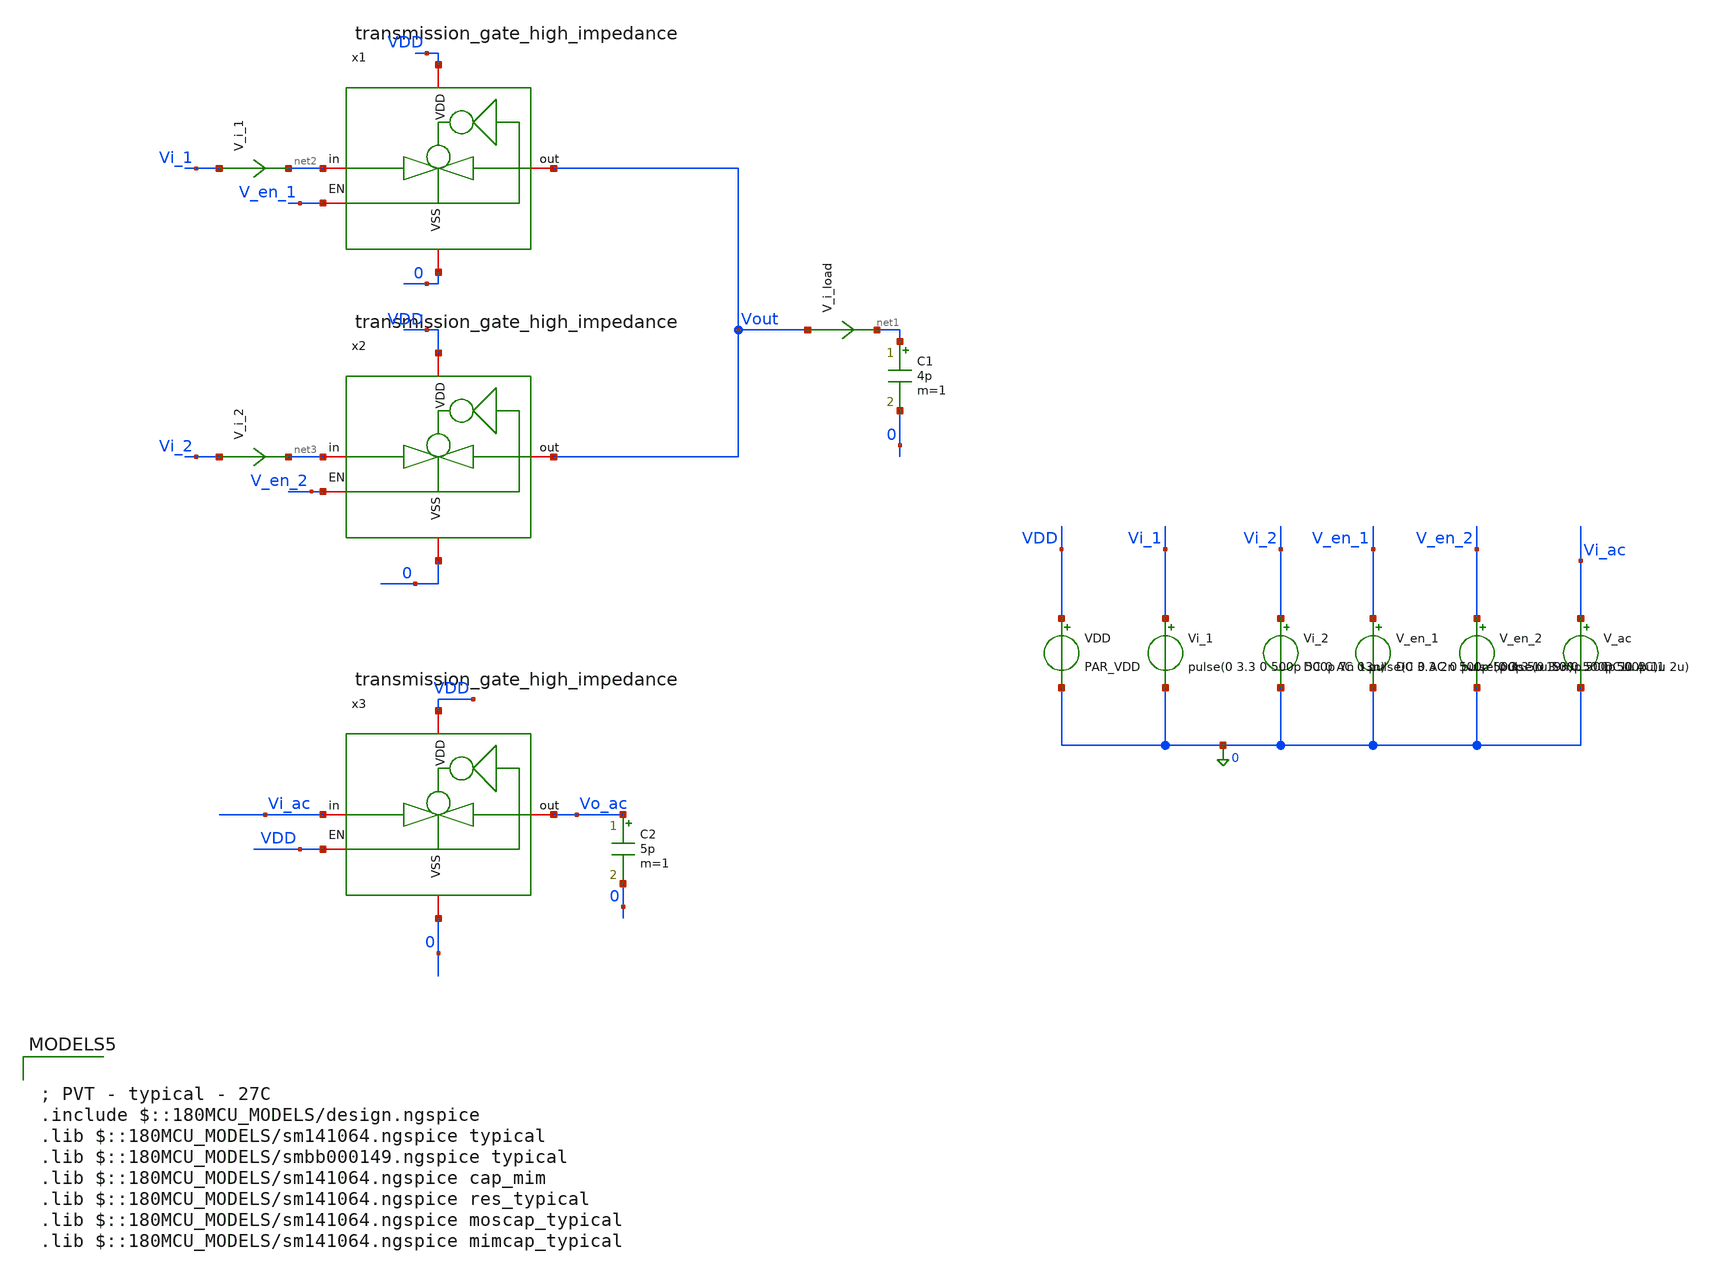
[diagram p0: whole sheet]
** sch_path: designs/digital/testbench/tb_transmission_gate_high_impedance_cross_talk.sch
**.subckt tb_transmission_gate_high_impedance_cross_talk
x1 VDD net2 Vout 0 V_en_1 transmission_gate_high_impedance
x2 VDD net3 Vout 0 V_en_2 transmission_gate_high_impedance
VDD VDD 0 PAR_VDD
Vi_1 Vi_1 0 pulse(0 3.3 0 500p 500p 7n 13n)
Vi_2 Vi_2 0 DC 0 AC 0 pulse(0 3.3 2n 500p 500p 5n 19n)
V_en_1 V_en_1 0 DC 0 AC 0 pulse(0 3.3 1u 500p 500p 1u 2u)
V_en_2 V_en_2 0 pulse(0 3.3 0 500p 500p 1u 2u)
V_i_load Vout net1 0
.save i(v_i_load)
V_i_1 Vi_1 net2 0
.save i(v_i_1)
V_i_2 Vi_2 net3 0
.save i(v_i_2)
C1 net1 0 4p m=1
V_ac Vi_ac 0 DC 0 AC 1
x3 VDD Vi_ac Vo_ac 0 VDD transmission_gate_high_impedance
C2 Vo_ac 0 5p m=1
**** begin user architecture code

; PVT - typical - 27C
.include $::180MCU_MODELS/design.ngspice
.lib $::180MCU_MODELS/sm141064.ngspice typical
.lib $::180MCU_MODELS/smbb000149.ngspice typical
.lib $::180MCU_MODELS/sm141064.ngspice cap_mim
.lib $::180MCU_MODELS/sm141064.ngspice res_typical
.lib $::180MCU_MODELS/sm141064.ngspice moscap_typical
.lib $::180MCU_MODELS/sm141064.ngspice mimcap_typical



** PARAMS

.PARAM PAR_VDD=3.3

.control
destroy all
save all

write tb_transmission_gate_high_impedance_cross_talk.raw

tran 0.1n 10u

plot vi_1 vi_2 v_en_1 v_en_2 vout xlimit 20n 40n
plot i(v_i_1) i(v_i_2) i(v_i_load) xlimit 20n 40n

ac dec 10 1 10G
plot vdb(vo_ac) vs frequency
meas ac f_3db when vdb(vo_ac)=-3
.endc


**** end user architecture code
**.ends

* expanding   symbol:  digital/schematic/transmission_gate_high_impedance.sym # of pins=5
** sym_path: designs/digital/schematic/transmission_gate_high_impedance.sym
** sch_path: designs/digital/schematic/transmission_gate_high_impedance.sch
.subckt transmission_gate_high_impedance VDD in out VSS EN
*.iopin VDD
*.iopin VSS
*.iopin in
*.iopin out
*.iopin EN
XM1 in net1 out VDD pfet_03v3 L=0.28u W=6u nf=1 ad='int((nf+1)/2) * W/nf * 0.18u' as='int((nf+2)/2) * W/nf * 0.18u'
+ pd='2*int((nf+1)/2) * (W/nf + 0.18u)' ps='2*int((nf+2)/2) * (W/nf + 0.18u)' nrd='0.18u / W' nrs='0.18u / W'
+ sa=0 sb=0 sd=0 m=1
XM2 in EN out VSS nfet_03v3 L=0.28u W=3u nf=1 ad='int((nf+1)/2) * W/nf * 0.18u' as='int((nf+2)/2) * W/nf * 0.18u'
+ pd='2*int((nf+1)/2) * (W/nf + 0.18u)' ps='2*int((nf+2)/2) * (W/nf + 0.18u)' nrd='0.18u / W' nrs='0.18u / W'
+ sa=0 sb=0 sd=0 m=1
XM3 net1 in VDD VDD nfet_03v3 L=0.28u W=1u nf=1 ad='int((nf+1)/2) * W/nf * 0.18u' as='int((nf+2)/2) * W/nf * 0.18u'
+ pd='2*int((nf+1)/2) * (W/nf + 0.18u)' ps='2*int((nf+2)/2) * (W/nf + 0.18u)' nrd='0.18u / W' nrs='0.18u / W'
+ sa=0 sb=0 sd=0 m=1
XM4 net1 in VSS VSS nfet_03v3 L=0.28u W=1u nf=1 ad='int((nf+1)/2) * W/nf * 0.18u' as='int((nf+2)/2) * W/nf * 0.18u'
+ pd='2*int((nf+1)/2) * (W/nf + 0.18u)' ps='2*int((nf+2)/2) * (W/nf + 0.18u)' nrd='0.18u / W' nrs='0.18u / W'
+ sa=0 sb=0 sd=0 m=1
.ends

.end
